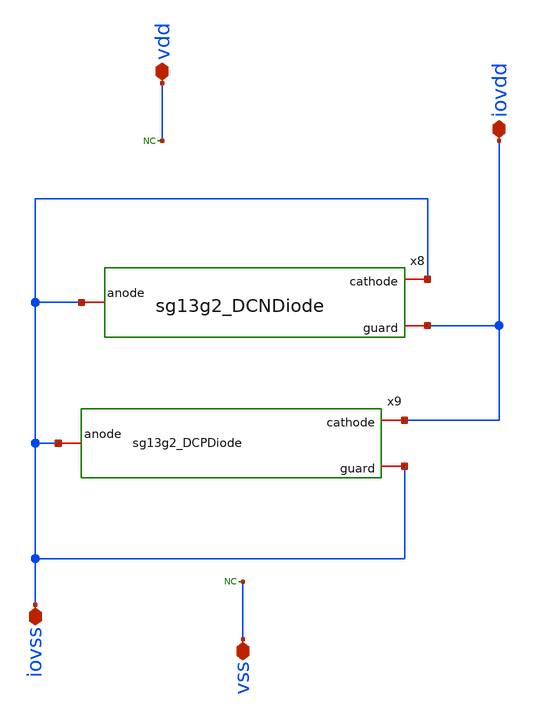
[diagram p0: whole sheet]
** sch_path: design/blocks-std/sg13g2_IOPadIOVss/schematic/sg13g2_IOPadIOVss.sch
**.subckt sg13g2_IOPadIOVss iovss iovdd vdd vss
*.iopin iovss
*.iopin iovdd
*.iopin vdd
*.iopin vss
x8 iovss iovss iovdd sg13g2_DCNDiode
x9 iovdd iovss iovss sg13g2_DCPDiode
* noconn vdd
* noconn vss
**.ends

* expanding   symbol:  blocks-std/sg13g2_DCNDiode/schematic/sg13g2_DCNDiode.sym # of pins=3
** sym_path: blocks-std/sg13g2_DCNDiode/schematic/sg13g2_DCNDiode.sym
** sch_path: blocks-std/sg13g2_DCNDiode/schematic/sg13g2_DCNDiode.sch
.subckt sg13g2_DCNDiode cathode anode guard
*.iopin cathode
*.iopin anode
*.iopin guard
XD1 anode cathode dantenna l=1.26u w=27.78u
XD2 anode cathode dantenna l=1.26u w=27.78u
.ends


* expanding   symbol:  blocks-std/sg13g2_DCPDiode/schematic/sg13g2_DCPDiode.sym # of pins=3
** sym_path: blocks-std/sg13g2_DCPDiode/schematic/sg13g2_DCPDiode.sym
** sch_path: blocks-std/sg13g2_DCPDiode/schematic/sg13g2_DCPDiode.sch
.subckt sg13g2_DCPDiode cathode anode guard
*.iopin cathode
*.iopin anode
*.iopin guard
XD1 anode cathode dpantenna l=1.26u w=27.78u
XD2 anode cathode dpantenna l=1.26u w=27.78u
.ends

.end
